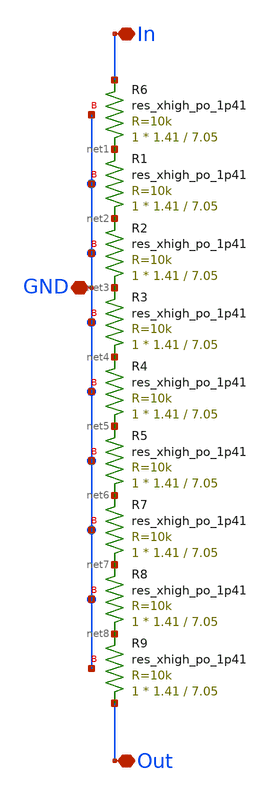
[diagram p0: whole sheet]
** sch_path: OTAs/NMOS_FoldedCasc_SE_OTA_IntBias/SCH/Res_70K.sch
**.subckt Res_70K In Out GND
*.iopin In
*.iopin Out
*.iopin GND
XR6 net1 In GND sky130_fd_pr__res_xhigh_po_1p41 L=7.05 mult=1 m=1
XR1 net2 net1 GND sky130_fd_pr__res_xhigh_po_1p41 L=7.05 mult=1 m=1
XR2 net3 net2 GND sky130_fd_pr__res_xhigh_po_1p41 L=7.05 mult=1 m=1
XR3 net4 net3 GND sky130_fd_pr__res_xhigh_po_1p41 L=7.05 mult=1 m=1
XR4 net5 net4 GND sky130_fd_pr__res_xhigh_po_1p41 L=7.05 mult=1 m=1
XR5 net6 net5 GND sky130_fd_pr__res_xhigh_po_1p41 L=7.05 mult=1 m=1
XR7 net7 net6 GND sky130_fd_pr__res_xhigh_po_1p41 L=7.05 mult=1 m=1
XR8 net8 net7 GND sky130_fd_pr__res_xhigh_po_1p41 L=7.05 mult=1 m=1
XR9 Out net8 GND sky130_fd_pr__res_xhigh_po_1p41 L=7.05 mult=1 m=1
**.ends
.end
